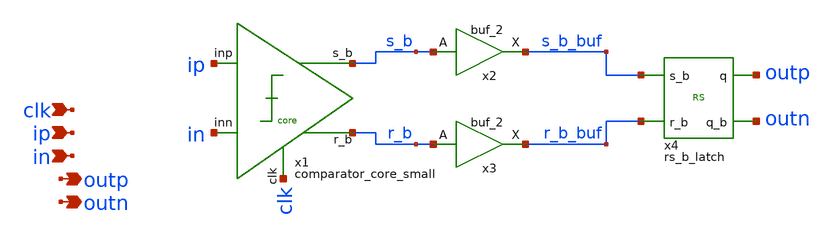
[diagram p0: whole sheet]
** sch_path: design/analog_modulator/schematic/comparator.sch
**.subckt comparator clk ip in outp outn
*.ipin clk
*.ipin ip
*.ipin in
*.opin outp
*.opin outn
x1 ip in s_b clk r_b VDD GND comparator_core_small
x2 s_b GND GND VDD VDD s_b_buf sky130_fd_sc_hd__buf_2
x3 r_b GND GND VDD VDD r_b_buf sky130_fd_sc_hd__buf_2
x4 s_b_buf r_b_buf outp outn VDD GND rs_b_latch
**.ends

* expanding   symbol:  comparator_core_small.sym # of pins=5
** sym_path: design/schematic/comparator_core_small.sym
** sch_path: design/schematic/comparator_core_small.sch
.subckt comparator_core_small inp inn s_b clk r_b VDD VSS
*.ipin clk
*.ipin inp
*.ipin inn
*.opin s_b
*.opin r_b
XM1 net1 clk VSS VSS sky130_fd_pr__nfet_01v8 L=0.15 W=4 nf=1 ad='int((nf+1)/2) * W/nf * 0.29' as='int((nf+2)/2) * W/nf * 0.29'
+ pd='2*int((nf+1)/2) * (W/nf + 0.29)' ps='2*int((nf+2)/2) * (W/nf + 0.29)' nrd='0.29 / W' nrs='0.29 / W'
+ sa=0 sb=0 sd=0 mult=1 m=1
XM2 p inp net1 VSS sky130_fd_pr__nfet_01v8 L=0.15 W=2 nf=1 ad='int((nf+1)/2) * W/nf * 0.29' as='int((nf+2)/2) * W/nf * 0.29'
+ pd='2*int((nf+1)/2) * (W/nf + 0.29)' ps='2*int((nf+2)/2) * (W/nf + 0.29)' nrd='0.29 / W' nrs='0.29 / W'
+ sa=0 sb=0 sd=0 mult=1 m=1
XM3 q inn net1 VSS sky130_fd_pr__nfet_01v8 L=0.15 W=2 nf=1 ad='int((nf+1)/2) * W/nf * 0.29' as='int((nf+2)/2) * W/nf * 0.29'
+ pd='2*int((nf+1)/2) * (W/nf + 0.29)' ps='2*int((nf+2)/2) * (W/nf + 0.29)' nrd='0.29 / W' nrs='0.29 / W'
+ sa=0 sb=0 sd=0 mult=1 m=1
XM4 s_b r_b p VSS sky130_fd_pr__nfet_01v8 L=0.15 W=1 nf=1 ad='int((nf+1)/2) * W/nf * 0.29' as='int((nf+2)/2) * W/nf * 0.29'
+ pd='2*int((nf+1)/2) * (W/nf + 0.29)' ps='2*int((nf+2)/2) * (W/nf + 0.29)' nrd='0.29 / W' nrs='0.29 / W'
+ sa=0 sb=0 sd=0 mult=1 m=1
XM5 r_b s_b q VSS sky130_fd_pr__nfet_01v8 L=0.15 W=1 nf=1 ad='int((nf+1)/2) * W/nf * 0.29' as='int((nf+2)/2) * W/nf * 0.29'
+ pd='2*int((nf+1)/2) * (W/nf + 0.29)' ps='2*int((nf+2)/2) * (W/nf + 0.29)' nrd='0.29 / W' nrs='0.29 / W'
+ sa=0 sb=0 sd=0 mult=1 m=1
XM6 s_b r_b VDD VDD sky130_fd_pr__pfet_01v8 L=0.15 W=2 nf=1 ad='int((nf+1)/2) * W/nf * 0.29' as='int((nf+2)/2) * W/nf * 0.29'
+ pd='2*int((nf+1)/2) * (W/nf + 0.29)' ps='2*int((nf+2)/2) * (W/nf + 0.29)' nrd='0.29 / W' nrs='0.29 / W'
+ sa=0 sb=0 sd=0 mult=1 m=1
XM7 r_b s_b VDD VDD sky130_fd_pr__pfet_01v8 L=0.15 W=2 nf=1 ad='int((nf+1)/2) * W/nf * 0.29' as='int((nf+2)/2) * W/nf * 0.29'
+ pd='2*int((nf+1)/2) * (W/nf + 0.29)' ps='2*int((nf+2)/2) * (W/nf + 0.29)' nrd='0.29 / W' nrs='0.29 / W'
+ sa=0 sb=0 sd=0 mult=1 m=1
XM8 s_b clk VDD VDD sky130_fd_pr__pfet_01v8 L=0.15 W=0.5 nf=1 ad='int((nf+1)/2) * W/nf * 0.29' as='int((nf+2)/2) * W/nf * 0.29'
+ pd='2*int((nf+1)/2) * (W/nf + 0.29)' ps='2*int((nf+2)/2) * (W/nf + 0.29)' nrd='0.29 / W' nrs='0.29 / W'
+ sa=0 sb=0 sd=0 mult=1 m=1
XM9 r_b clk VDD VDD sky130_fd_pr__pfet_01v8 L=0.15 W=0.5 nf=1 ad='int((nf+1)/2) * W/nf * 0.29' as='int((nf+2)/2) * W/nf * 0.29'
+ pd='2*int((nf+1)/2) * (W/nf + 0.29)' ps='2*int((nf+2)/2) * (W/nf + 0.29)' nrd='0.29 / W' nrs='0.29 / W'
+ sa=0 sb=0 sd=0 mult=1 m=1
XM10 p clk VDD VDD sky130_fd_pr__pfet_01v8 L=0.15 W=0.5 nf=1 ad='int((nf+1)/2) * W/nf * 0.29' as='int((nf+2)/2) * W/nf * 0.29'
+ pd='2*int((nf+1)/2) * (W/nf + 0.29)' ps='2*int((nf+2)/2) * (W/nf + 0.29)' nrd='0.29 / W' nrs='0.29 / W'
+ sa=0 sb=0 sd=0 mult=1 m=1
XM11 q clk VDD VDD sky130_fd_pr__pfet_01v8 L=0.15 W=0.5 nf=1 ad='int((nf+1)/2) * W/nf * 0.29' as='int((nf+2)/2) * W/nf * 0.29'
+ pd='2*int((nf+1)/2) * (W/nf + 0.29)' ps='2*int((nf+2)/2) * (W/nf + 0.29)' nrd='0.29 / W' nrs='0.29 / W'
+ sa=0 sb=0 sd=0 mult=1 m=1
.ends


* expanding   symbol:  rs_b_latch.sym # of pins=4
** sym_path: design/analog_modulator/schematic/rs_b_latch.sym
** sch_path: design/analog_modulator/schematic/rs_b_latch.sch
.subckt rs_b_latch s_b r_b q q_b VDD VSS
*.ipin s_b
*.ipin r_b
*.opin q
*.opin q_b
x1 s_b q_b VSS VSS VDD VDD q sky130_fd_sc_hd__nand2_4
x2 r_b q VSS VSS VDD VDD q_b sky130_fd_sc_hd__nand2_4
.ends

.GLOBAL VDD
.end
